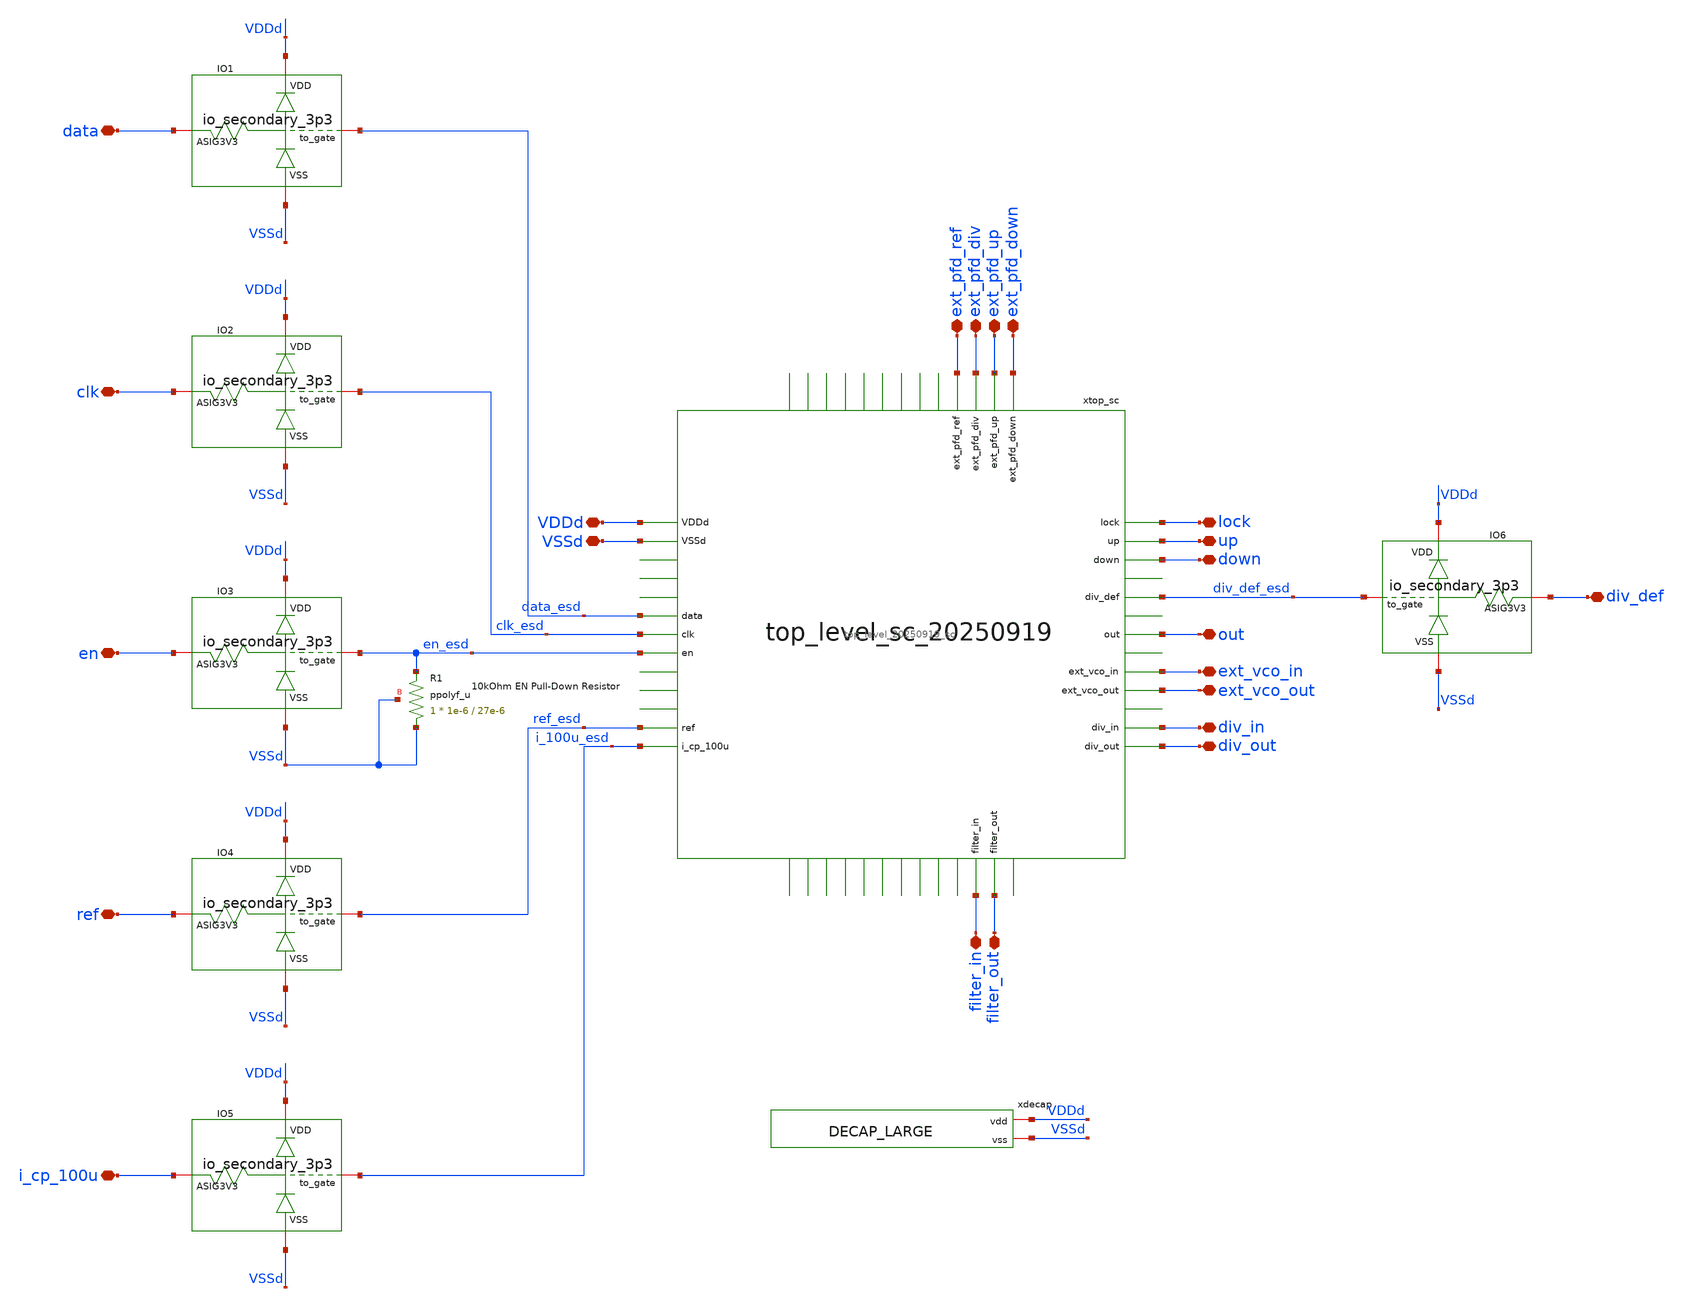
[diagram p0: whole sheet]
** sch_path: designs/libs/top_level/top_level_20250919/top_level_20250919_final/top_level_20250919_final.sch
**.subckt top_level_20250919_final VDDd VSSd ref i_cp_100u filter_in filter_out ext_pfd_ref
*+ ext_pfd_up ext_pfd_down ext_pfd_div up down out lock ext_vco_out ext_vco_in div_out div_in data clk en div_def
*.iopin VDDd
*.iopin VSSd
*.iopin ref
*.iopin i_cp_100u
*.iopin filter_in
*.iopin filter_out
*.iopin ext_pfd_ref
*.iopin ext_pfd_up
*.iopin ext_pfd_down
*.iopin ext_pfd_div
*.iopin up
*.iopin down
*.iopin out
*.iopin lock
*.iopin ext_vco_out
*.iopin ext_vco_in
*.iopin div_out
*.iopin div_in
*.iopin data
*.iopin clk
*.iopin en
*.iopin div_def
xtop_sc VDDd VSSd data_esd clk_esd en_esd ref_esd i_100u_esd ext_pfd_ref ext_pfd_div ext_pfd_up
+ ext_pfd_down lock up down filter_out ext_vco_in div_in div_out out filter_in ext_vco_out div_def_esd
+ top_level_20250919_sc
XR1 VSSd en_esd VSSd ppolyf_u r_width=1e-6 r_length=27e-6 m=1
XIO1 VDDd data_esd data VSSd io_secondary_3p3
XIO2 VDDd clk_esd clk VSSd io_secondary_3p3
XIO3 VDDd en_esd en VSSd io_secondary_3p3
XIO4 VDDd ref_esd ref VSSd io_secondary_3p3
XIO5 VDDd i_100u_esd i_cp_100u VSSd io_secondary_3p3
XIO6 VDDd div_def_esd div_def VSSd io_secondary_3p3
xdecap VDDd VSSd DECAP_LARGE
**.ends
.end
